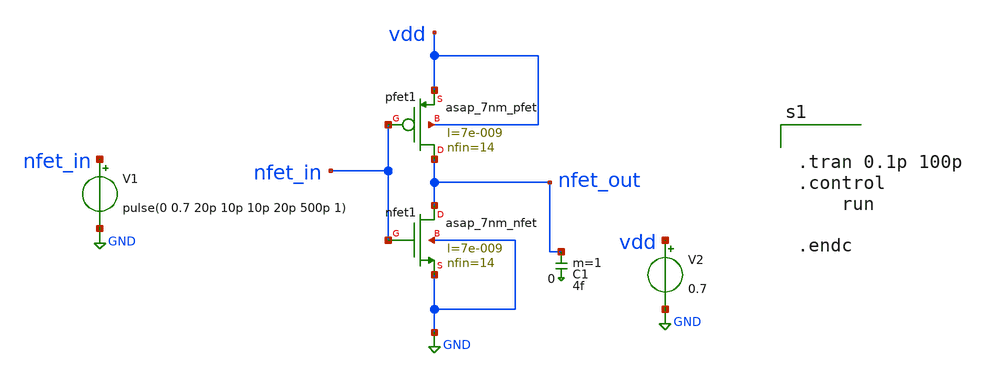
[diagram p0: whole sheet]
** sch_path: inverter_VTC.sch
**.subckt inverter_VTC
Xpfet1 nfet_out nfet_in vdd vdd asap_7nm_pfet l=7e-009 nfin=14
Xnfet1 nfet_out nfet_in GND GND asap_7nm_nfet l=7e-009 nfin=14
V1 nfet_in GND pulse(0 0.7 20p 10p 10p 20p 500p 1)
V2 vdd GND 0.7
C1 nfet_out 0 4f m=1
**** begin user architecture code


.tran 0.1p 100p
.control
    run

.endc


**** end user architecture code
**.ends
.GLOBAL GND
.end
